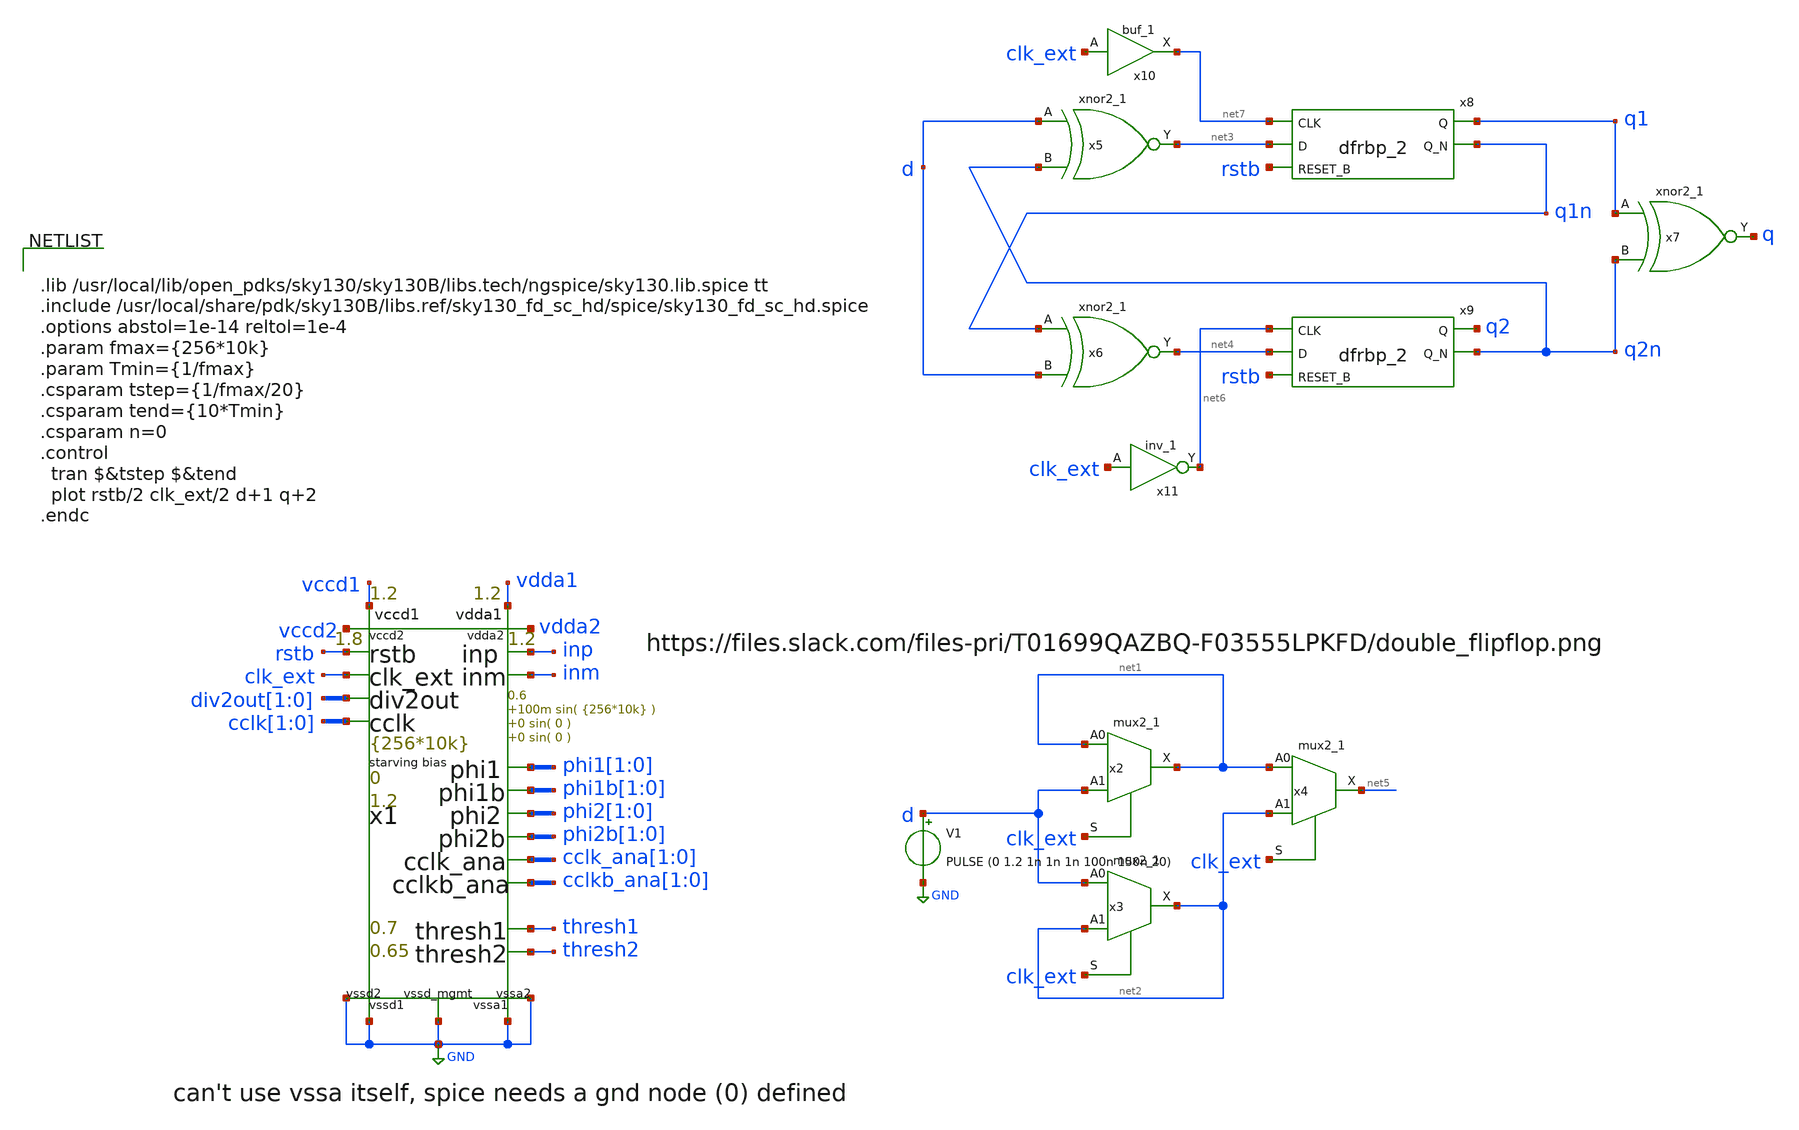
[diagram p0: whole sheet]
** sch_path: xschem/test_bench/detff_ss_tb.sch
**.subckt detff_ss_tb
x1 thresh1 thresh2 inp inm clk_ext rstb phi1[1] phi1[0] phi1b[1] phi1b[0] phi2[1] phi2[0] phi2b[1] phi2b[0]
+ cclk_ana[1] cclk_ana[0] cclkb_ana[1] cclkb_ana[0] div2out[1] div2out[0] cclk[1] cclk[0] vdda1 vccd1 vccd2
+ vdda2 GND GND GND GND GND risc_signals p_vdda1=1.2 p_vdda2=1.2 p_vccd1=1.2 p_vccd2=1.8 p_vccd_mgmt=1.8
+ p_fclk={256*10k} p_duty_cycle=0.5 p_rstb_delay={1.5/p_fclk} p_rstb_tr=5n p_thresh1=0.7 p_thresh2=0.65
+ p_vpb=0 p_vnb=1.2 p_vcm=0.6 p_amp1=100m p_f1={256*10k} p_amp2=0 p_f2=0 p_amp3=0 p_f3=0
x2 net1 d clk_ext GND GND vccd1 vccd1 net1 sky130_fd_sc_hd__mux2_1
x3 d net2 clk_ext GND GND vccd1 vccd1 net2 sky130_fd_sc_hd__mux2_1
x4 net1 net2 clk_ext GND GND vccd1 vccd1 net5 sky130_fd_sc_hd__mux2_1
V1 d GND PULSE (0 1.2 1n 1n 1n 100n 150n 20)
x5 d q2n gnd gnd vccd1 vccd1 net3 sky130_fd_sc_hd__xnor2_1
x8 net7 net3 rstb gnd gnd vccd1 vccd1 q1 q1n sky130_fd_sc_hd__dfrbp_2
x10 clk_ext gnd gnd vccd1 vccd1 net7 sky130_fd_sc_hd__buf_1
x11 clk_ext gnd gnd vccd1 vccd1 net6 sky130_fd_sc_hd__inv_1
x6 q1n d gnd gnd vccd1 vccd1 net4 sky130_fd_sc_hd__xnor2_1
x7 q1 q2n gnd gnd vccd1 vccd1 q sky130_fd_sc_hd__xnor2_1
x9 net6 net4 rstb gnd gnd vccd1 vccd1 q2 q2n sky130_fd_sc_hd__dfrbp_2
**** begin user architecture code


.lib /usr/local/lib/open_pdks/sky130/sky130B/libs.tech/ngspice/sky130.lib.spice tt
.include /usr/local/share/pdk/sky130B/libs.ref/sky130_fd_sc_hd/spice/sky130_fd_sc_hd.spice
.options abstol=1e-14 reltol=1e-4
.param fmax={256*10k}
.param Tmin={1/fmax}
.csparam tstep={1/fmax/20}
.csparam tend={10*Tmin}
.csparam n=0
.control
  tran $&tstep $&tend
  plot rstb/2 clk_ext/2 d+1 q+2
.endc


**** end user architecture code
**.ends
.GLOBAL GND
.end
